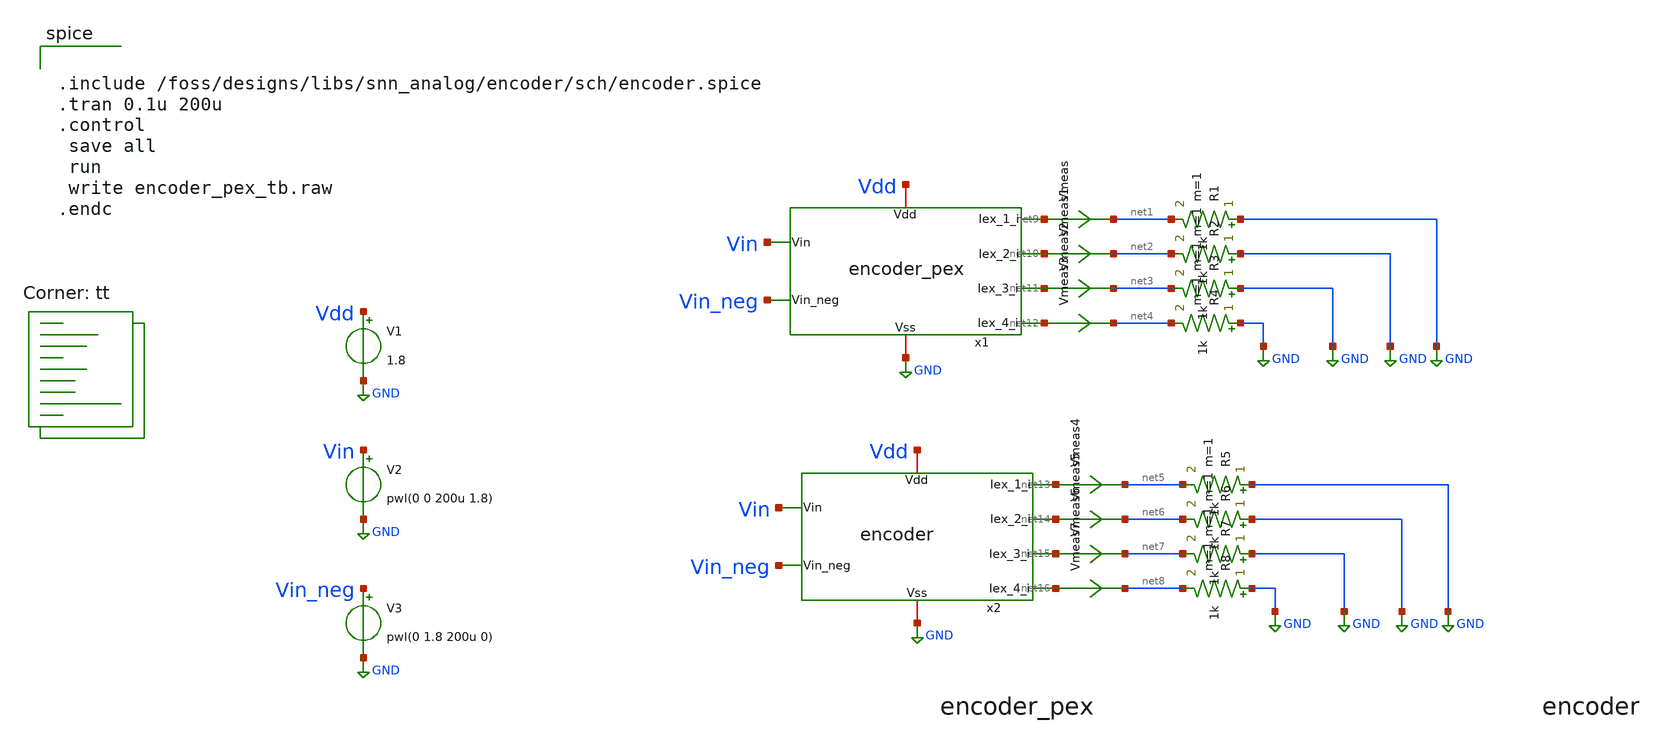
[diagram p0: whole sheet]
** sch_path: designs/libs/snn_analog/encoder/sch/encoder_pex_tb.sch
**.subckt encoder_pex_tb
R1 GND net1 1k m=1
R2 GND net2 1k m=1
R3 GND net3 1k m=1
R4 GND net4 1k m=1
Vmeas net9 net1 0
.save i(vmeas)
Vmeas1 net10 net2 0
.save i(vmeas1)
Vmeas2 net11 net3 0
.save i(vmeas2)
Vmeas3 net12 net4 0
.save i(vmeas3)
V1 Vdd GND 1.8
V2 Vin GND pwl(0 0 200u 1.8)
V3 Vin_neg GND pwl(0 1.8 200u 0)
x1 Vdd GND Vin Vin_neg net9 net10 net11 net12 encoder_pex
x2 Vdd GND Vin Vin_neg net13 net14 net15 net16 encoder
R5 GND net5 1k m=1
R6 GND net6 1k m=1
R7 GND net7 1k m=1
R8 GND net8 1k m=1
Vmeas4 net13 net5 0
.save i(vmeas4)
Vmeas5 net14 net6 0
.save i(vmeas5)
Vmeas6 net15 net7 0
.save i(vmeas6)
Vmeas7 net16 net8 0
.save i(vmeas7)
**** begin user architecture code


.include /foss/designs/libs/snn_analog/encoder/sch/encoder.spice
.tran 0.1u 200u
.control
 save all
 run
 write encoder_pex_tb.raw
.endc

.lib $::SKYWATER_MODELS/sky130.lib.spice tt
**** end user architecture code
**.ends

* expanding   symbol:  encoder.sym # of pins=8
** sym_path: designs/libs/snn_analog/encoder/sch/encoder.sym
** sch_path: designs/libs/snn_analog/encoder/sch/encoder.sch
.subckt encoder Vdd Vss Vin Vin_neg Iex_1_i Iex_2_i Iex_3_i Iex_4_i
*.iopin Vdd
*.iopin Vss
*.ipin Vin
*.ipin Vin_neg
*.opin Iex_1_i
*.opin Iex_4_i
*.opin Iex_2_i
*.opin Iex_3_i
XM1 x Vin a Vss sky130_fd_pr__nfet_01v8 L=10 W=0.5 nf=1 ad='int((1 + 1)/2) * 0.5 / 1 * 0.29' as='int((1 + 2)/2) * 0.5 / 1 * 0.29'
+ pd='2*int((1 + 1)/2) * (0.5 / 1 + 0.29)' ps='2*int((1 + 2)/2) * (0.5 / 1 + 0.29)' nrd='0.29 / 0.5 ' nrs='0.29 / 0.5 '
+ sa=0 sb=0 sd=0 mult=1 m=1
XM2 y Vin_neg a Vss sky130_fd_pr__nfet_01v8 L=10 W=0.5 nf=1 ad='int((1 + 1)/2) * 0.5 / 1 * 0.29' as='int((1 + 2)/2) * 0.5 / 1 * 0.29'
+ pd='2*int((1 + 1)/2) * (0.5 / 1 + 0.29)' ps='2*int((1 + 2)/2) * (0.5 / 1 + 0.29)' nrd='0.29 / 0.5 ' nrs='0.29 / 0.5 '
+ sa=0 sb=0 sd=0 mult=1 m=1
XM3 x x Vdd Vdd sky130_fd_pr__pfet_01v8 L=0.28 W=2 nf=1 ad='int((1 + 1)/2) * 2 / 1 * 0.29' as='int((1 + 2)/2) * 2 / 1 * 0.29'
+ pd='2*int((1 + 1)/2) * (2 / 1 + 0.29)' ps='2*int((1 + 2)/2) * (2 / 1 + 0.29)' nrd='0.29 / 2 ' nrs='0.29 / 2 '
+ sa=0 sb=0 sd=0 mult=1 m=1
XM4 y y Vdd Vdd sky130_fd_pr__pfet_01v8 L=0.28 W=2 nf=1 ad='int((1 + 1)/2) * 2 / 1 * 0.29' as='int((1 + 2)/2) * 2 / 1 * 0.29'
+ pd='2*int((1 + 1)/2) * (2 / 1 + 0.29)' ps='2*int((1 + 2)/2) * (2 / 1 + 0.29)' nrd='0.29 / 2 ' nrs='0.29 / 2 '
+ sa=0 sb=0 sd=0 mult=1 m=1
XM5 Iex_2_i x Vdd Vdd sky130_fd_pr__pfet_01v8 L=0.94 W=0.5 nf=1 ad='int((1 + 1)/2) * 0.5 / 1 * 0.29'
+ as='int((1 + 2)/2) * 0.5 / 1 * 0.29' pd='2*int((1 + 1)/2) * (0.5 / 1 + 0.29)' ps='2*int((1 + 2)/2) * (0.5 / 1 + 0.29)'
+ nrd='0.29 / 0.5 ' nrs='0.29 / 0.5 ' sa=0 sb=0 sd=0 mult=1 m=1
XM6 Iex_4_i y Vdd Vdd sky130_fd_pr__pfet_01v8 L=0.94 W=0.5 nf=1 ad='int((1 + 1)/2) * 0.5 / 1 * 0.29'
+ as='int((1 + 2)/2) * 0.5 / 1 * 0.29' pd='2*int((1 + 1)/2) * (0.5 / 1 + 0.29)' ps='2*int((1 + 2)/2) * (0.5 / 1 + 0.29)'
+ nrd='0.29 / 0.5 ' nrs='0.29 / 0.5 ' sa=0 sb=0 sd=0 mult=1 m=1
XM7 Iex_3_i y Vdd Vdd sky130_fd_pr__pfet_01v8 L=0.94 W=0.5 nf=1 ad='int((1 + 1)/2) * 0.5 / 1 * 0.29'
+ as='int((1 + 2)/2) * 0.5 / 1 * 0.29' pd='2*int((1 + 1)/2) * (0.5 / 1 + 0.29)' ps='2*int((1 + 2)/2) * (0.5 / 1 + 0.29)'
+ nrd='0.29 / 0.5 ' nrs='0.29 / 0.5 ' sa=0 sb=0 sd=0 mult=1 m=1
XM8 Iex_1_i x Vdd Vdd sky130_fd_pr__pfet_01v8 L=0.94 W=0.5 nf=1 ad='int((1 + 1)/2) * 0.5 / 1 * 0.29'
+ as='int((1 + 2)/2) * 0.5 / 1 * 0.29' pd='2*int((1 + 1)/2) * (0.5 / 1 + 0.29)' ps='2*int((1 + 2)/2) * (0.5 / 1 + 0.29)'
+ nrd='0.29 / 0.5 ' nrs='0.29 / 0.5 ' sa=0 sb=0 sd=0 mult=1 m=1
XM9 a net1 Vss Vss sky130_fd_pr__nfet_01v8 L=1.12 W=2 nf=1 ad='int((1 + 1)/2) * 2 / 1 * 0.29' as='int((1 + 2)/2) * 2 / 1 * 0.29'
+ pd='2*int((1 + 1)/2) * (2 / 1 + 0.29)' ps='2*int((1 + 2)/2) * (2 / 1 + 0.29)' nrd='0.29 / 2 ' nrs='0.29 / 2 '
+ sa=0 sb=0 sd=0 mult=1 m=1
XM10 net1 net1 Vss Vss sky130_fd_pr__nfet_01v8 L=0.28 W=0.5 nf=1 ad='int((1 + 1)/2) * 0.5 / 1 * 0.29'
+ as='int((1 + 2)/2) * 0.5 / 1 * 0.29' pd='2*int((1 + 1)/2) * (0.5 / 1 + 0.29)' ps='2*int((1 + 2)/2) * (0.5 / 1 + 0.29)'
+ nrd='0.29 / 0.5 ' nrs='0.29 / 0.5 ' sa=0 sb=0 sd=0 mult=1 m=1
XM11 net1 net1 Vdd Vdd sky130_fd_pr__pfet_01v8 L=0.28 W=0.5 nf=1 ad='int((1 + 1)/2) * 0.5 / 1 * 0.29'
+ as='int((1 + 2)/2) * 0.5 / 1 * 0.29' pd='2*int((1 + 1)/2) * (0.5 / 1 + 0.29)' ps='2*int((1 + 2)/2) * (0.5 / 1 + 0.29)'
+ nrd='0.29 / 0.5 ' nrs='0.29 / 0.5 ' sa=0 sb=0 sd=0 mult=1 m=1
.ends

.GLOBAL GND
.end
